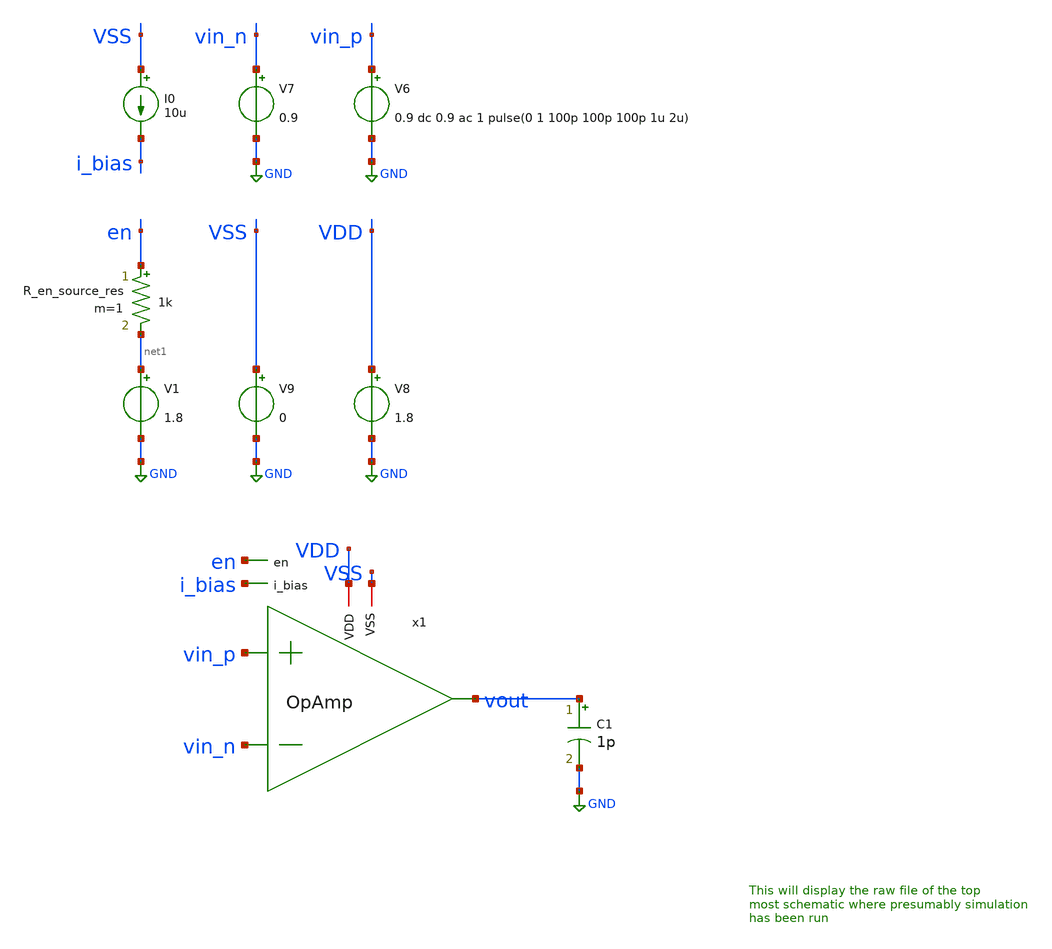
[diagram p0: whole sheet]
** sch_path: ISSCC_2025_V1/xschem/Benchmark_Circuits/test_analog/test_analog.sch
* Copyright 2021 Stefan Frederik Schippers
* Licensed under the Apache License, Version 2.0 (the "License");
* you may not use this file except in compliance with the License.
* You may obtain a copy of the License at
* https://www.apache.org/licenses/LICENSE-2.0
* Unless required by applicable law or agreed to in writing, software
* distributed under the License is distributed on an "AS IS" BASIS,
* WITHOUT WARRANTIES OR CONDITIONS OF ANY KIND, either express or implied.
* See the License for the specific language governing permissions and
* limitations under the License.
**.subckt test_analog
V6 vin_p GND 0.9 dc 0.9 ac 1 pulse(0 1 100p 100p 100p 1u 2u)
V7 vin_n GND 0.9
V8 VDD GND 1.8
V9 VSS GND 0
I0 VSS i_bias 10u
V1 net1 GND 1.8
C1 vout GND 1p m=1
R_en_source_res en net1 1k m=1
x1 VDD vout vin_p vin_n VSS i_bias en OpAmp
**** begin user architecture code

** opencircuitdesign pdks install
.lib /home/timothyjabez/Documents/Open_Source_Circuit_Design/Edited_Pdk/sky130A/libs.tech/combined/sky130.lib.spice tt


**** end user architecture code
**.ends

* expanding   symbol:  Benchmark_Circuits/OpAmp/OpAmp.sym # of pins=7
** sym_path: ISSCC_2025_V1/xschem/Benchmark_Circuits/OpAmp_Defect/OpAmp.sym
** sch_path: ISSCC_2025_V1/xschem/Benchmark_Circuits/OpAmp_Defect/OpAmp.sch
.subckt OpAmp VDD vout vin_p vin_n VSS i_bias en
*.ipin vin_p
*.ipin vin_n
*.iopin VSS
*.iopin VDD
*.opin vout
*.ipin i_bias
*.ipin en
XM1 vout Active_load_g VDD VDD sky130_fd_pr__pfet_01v8 L=1 W=8 nf=2 ad='int((nf+1)/2) * W/nf * 0.29'
+ as='int((nf+2)/2) * W/nf * 0.29' pd='2*int((nf+1)/2) * (W/nf + 0.29)' ps='2*int((nf+2)/2) * (W/nf + 0.29)'
+ nrd='0.29 / W' nrs='0.29 / W' sa=0 sb=0 sd=0 mult=1 m=1
XM2 Active_load_g Active_load_g VDD VDD sky130_fd_pr__pfet_01v8 L=1 W=8 nf=2 ad='int((nf+1)/2) * W/nf * 0.29'
+ as='int((nf+2)/2) * W/nf * 0.29' pd='2*int((nf+1)/2) * (W/nf + 0.29)' ps='2*int((nf+2)/2) * (W/nf + 0.29)'
+ nrd='0.29 / W' nrs='0.29 / W' sa=0 sb=0 sd=0 mult=1 m=1
XM3 Active_load_g vin_p I_mirror_d VSS sky130_fd_pr__nfet_01v8 L=0.5 W=16 nf=4 ad='int((nf+1)/2) * W/nf * 0.29'
+ as='int((nf+2)/2) * W/nf * 0.29' pd='2*int((nf+1)/2) * (W/nf + 0.29)' ps='2*int((nf+2)/2) * (W/nf + 0.29)'
+ nrd='0.29 / W' nrs='0.29 / W' sa=0 sb=0 sd=0 mult=1 m=1
XM4 vout vin_n I_mirror_d VSS sky130_fd_pr__nfet_01v8 L=0.5 W=16 nf=4 ad='int((nf+1)/2) * W/nf * 0.29'
+ as='int((nf+2)/2) * W/nf * 0.29' pd='2*int((nf+1)/2) * (W/nf + 0.29)' ps='2*int((nf+2)/2) * (W/nf + 0.29)'
+ nrd='0.29 / W' nrs='0.29 / W' sa=0 sb=0 sd=0 mult=1 m=1
XM5 I_mirror_d I_mirror_g VSS VSS sky130_fd_pr__nfet_01v8 L=1 W=8 nf=2 ad='int((nf+1)/2) * W/nf * 0.29'
+ as='int((nf+2)/2) * W/nf * 0.29' pd='2*int((nf+1)/2) * (W/nf + 0.29)' ps='2*int((nf+2)/2) * (W/nf + 0.29)'
+ nrd='0.29 / W' nrs='0.29 / W' sa=0 sb=0 sd=0 mult=2 m=2
XM6 i_bias I_mirror_g VSS VSS sky130_fd_pr__nfet_01v8 L=1 W=8 nf=2 ad='int((nf+1)/2) * W/nf * 0.29' as='int((nf+2)/2) * W/nf * 0.29'
+ pd='2*int((nf+1)/2) * (W/nf + 0.29)' ps='2*int((nf+2)/2) * (W/nf + 0.29)' nrd='0.29 / W' nrs='0.29 / W'
+ sa=0 sb=0 sd=0 mult=1 m=1
XM9 en_n en VDD VDD sky130_fd_pr__pfet_01v8 L=0.15 W=2 nf=1 ad='int((nf+1)/2) * W/nf * 0.29' as='int((nf+2)/2) * W/nf * 0.29'
+ pd='2*int((nf+1)/2) * (W/nf + 0.29)' ps='2*int((nf+2)/2) * (W/nf + 0.29)' nrd='0.29 / W' nrs='0.29 / W'
+ sa=0 sb=0 sd=0 mult=1 m=1
XM10 en_n en VSS VSS sky130_fd_pr__nfet_01v8 L=0.15 W=1 nf=1 ad='int((nf+1)/2) * W/nf * 0.29' as='int((nf+2)/2) * W/nf * 0.29'
+ pd='2*int((nf+1)/2) * (W/nf + 0.29)' ps='2*int((nf+2)/2) * (W/nf + 0.29)' nrd='0.29 / W' nrs='0.29 / W'
+ sa=0 sb=0 sd=0 mult=1 m=1
XM7 i_bias en I_mirror_g VSS sky130_fd_pr__nfet_01v8 L=0.35 W=4 nf=2 ad='int((nf+1)/2) * W/nf * 0.29'
+ as='int((nf+2)/2) * W/nf * 0.29' pd='2*int((nf+1)/2) * (W/nf + 0.29)' ps='2*int((nf+2)/2) * (W/nf + 0.29)'
+ nrd='0.29 / W' nrs='0.29 / W' sa=0 sb=0 sd=0 mult=1 m=1
XM8 I_mirror_g en_n VSS VSS sky130_fd_pr__nfet_01v8 L=0.35 W=4 nf=2 ad='int((nf+1)/2) * W/nf * 0.29'
+ as='int((nf+2)/2) * W/nf * 0.29' pd='2*int((nf+1)/2) * (W/nf + 0.29)' ps='2*int((nf+2)/2) * (W/nf + 0.29)'
+ nrd='0.29 / W' nrs='0.29 / W' sa=0 sb=0 sd=0 mult=1 m=1
XM11 Active_load_g en VDD VDD sky130_fd_pr__pfet_01v8 L=0.35 W=4 nf=2 ad='int((nf+1)/2) * W/nf * 0.29'
+ as='int((nf+2)/2) * W/nf * 0.29' pd='2*int((nf+1)/2) * (W/nf + 0.29)' ps='2*int((nf+2)/2) * (W/nf + 0.29)'
+ nrd='0.29 / W' nrs='0.29 / W' sa=0 sb=0 sd=0 mult=1 m=1
R_open en I_mirror_g 1 m=1
.ends

.GLOBAL GND
**** begin user architecture code


* ngspice commands
.options savecurrents

.control
save all

op
remzerovec

tran 100n 10u
plot v(vout)

let trise_pulse = 999
meas tran trise_pulse TRIG v(vout) VAL=0.1*1.8 RISE=1 TARG v(vout) VAL=0.9*1.8 RISE=1
let slew_rate = 0.8*1.8/trise_pulse
print slew_rate > ./specs/opamp_specs.txt
let power_consumption = -@V8[i]*v(VDD)
meas tran power_average AVG power_consumption from=0u to=10u
print power_average >> ./specs/opamp_specs.txt
;write top_level.out

set appendwrite
set units=degrees
dc V6 0 1.8 0.01
remzerovec
;write top_level.out

ac dec 10 1 1e12
let gain = v(vout)/(v(vin_p)-v(vin_n))

; Measurement of OpAmp performance parameters
let AOL_DC_dB = 0
meas ac AOL_DC_dB FIND vdb(gain) AT=10
print AOL_DC_dB >> ./specs/opamp_specs.txt
let gain_3dB = AOL_DC_dB-3
print gain_3dB
let BW3dB = 0
meas ac BW3dB when vdb(gain) = gain_3dB
print BW3dB >> ./specs/opamp_specs.txt
let UGBW = 0
meas ac UGBW when vdb(gain) = 1
print UGBW >> ./specs/opamp_specs.txt
let Phase_Unity_Gain = -999
meas ac Phase_Unity_Gain FIND vp(gain) AT=UGBW
meas ac Zero_PM_Freq when vp(gain)=-175
let Gain_Margin = 999
meas ac Gain_Margin FIND vdb(gain) at=Zero_PM_Freq
print Gain_margin >> ./specs/opamp_specs.txt
let Phase_Margin = 180+Phase_Unity_Gain
print Phase_Margin >> ./specs/opamp_specs.txt

settype decibel gain
plot vdb(gain) ylabel 'gain mag'
plot cph(gain) ylabel 'gain phase'
;write top_level.out
.endc



**** end user architecture code
.end
